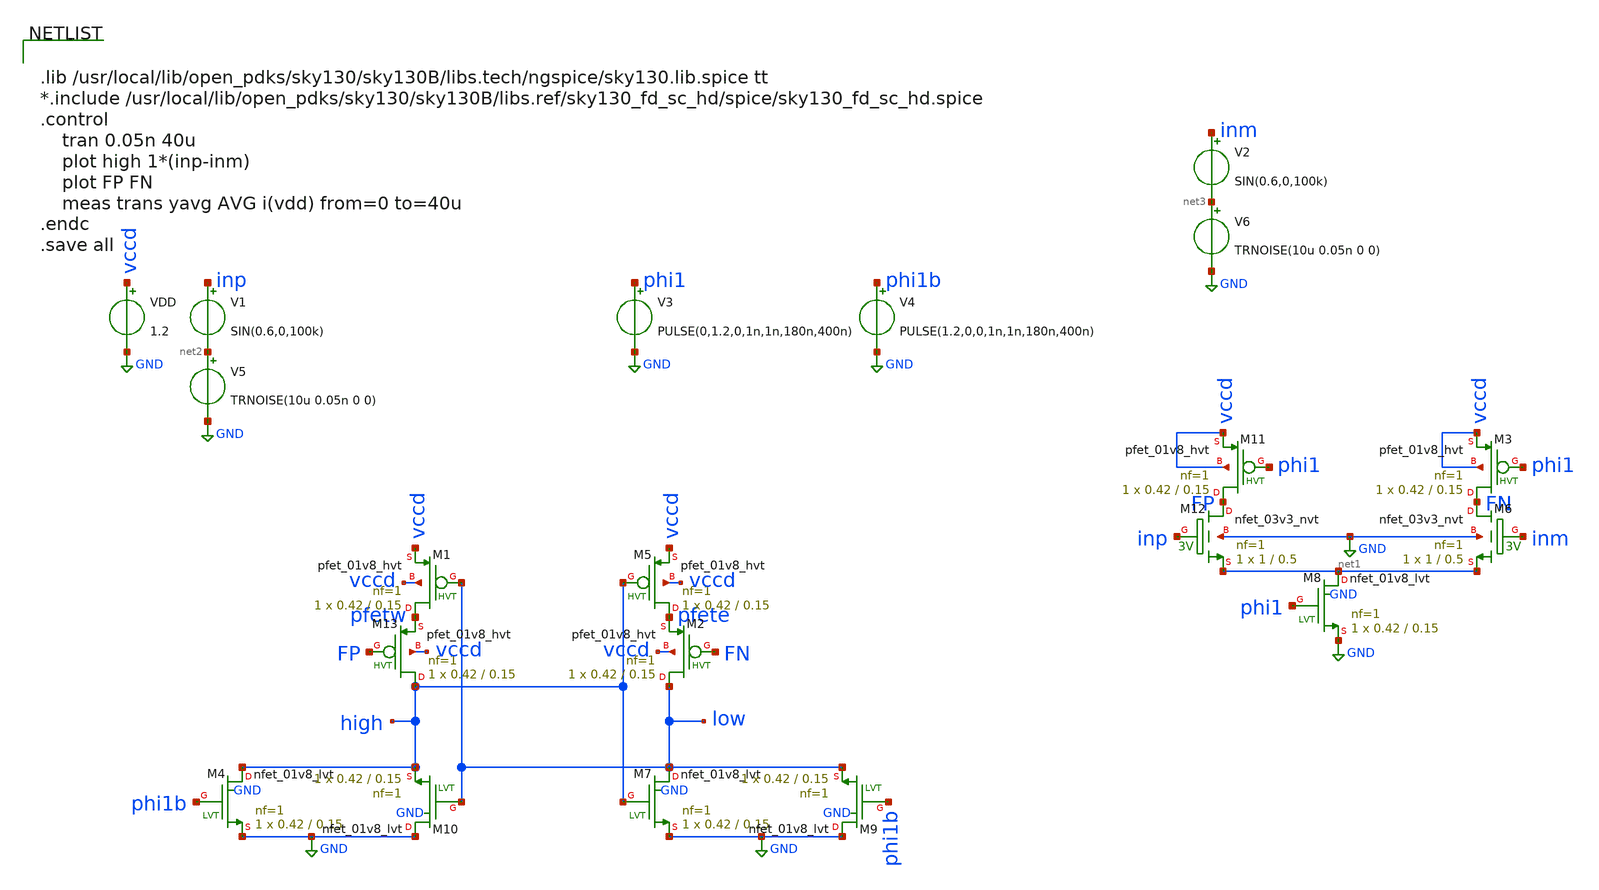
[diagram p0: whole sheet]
** sch_path: xschem/test_bench/comparator_tb.sch
**.subckt comparator_tb
V1 inp net2 SIN(0.6,0,100k)
VDD vccd GND 1.2
V2 inm net3 SIN(0.6,0,100k)
V3 phi1 GND PULSE(0,1.2,0,1n,1n,180n,400n)
V4 phi1b GND PULSE(1.2,0,0,1n,1n,180n,400n)
XM4 high phi1b GND GND sky130_fd_pr__nfet_01v8_lvt L=0.15 W=0.42 nf=1 ad='int((nf+1)/2) * W/nf * 0.29'
+ as='int((nf+2)/2) * W/nf * 0.29' pd='2*int((nf+1)/2) * (W/nf + 0.29)' ps='2*int((nf+2)/2) * (W/nf + 0.29)'
+ nrd='0.29 / W' nrs='0.29 / W' sa=0 sb=0 sd=0 mult=1 m=1
XM7 low high GND GND sky130_fd_pr__nfet_01v8_lvt L=0.15 W=0.42 nf=1 ad='int((nf+1)/2) * W/nf * 0.29'
+ as='int((nf+2)/2) * W/nf * 0.29' pd='2*int((nf+1)/2) * (W/nf + 0.29)' ps='2*int((nf+2)/2) * (W/nf + 0.29)'
+ nrd='0.29 / W' nrs='0.29 / W' sa=0 sb=0 sd=0 mult=1 m=1
XM9 GND phi1b low GND sky130_fd_pr__nfet_01v8_lvt L=0.15 W=0.42 nf=1 ad='int((nf+1)/2) * W/nf * 0.29'
+ as='int((nf+2)/2) * W/nf * 0.29' pd='2*int((nf+1)/2) * (W/nf + 0.29)' ps='2*int((nf+2)/2) * (W/nf + 0.29)'
+ nrd='0.29 / W' nrs='0.29 / W' sa=0 sb=0 sd=0 mult=1 m=1
XM10 GND low high GND sky130_fd_pr__nfet_01v8_lvt L=0.15 W=0.42 nf=1 ad='int((nf+1)/2) * W/nf * 0.29'
+ as='int((nf+2)/2) * W/nf * 0.29' pd='2*int((nf+1)/2) * (W/nf + 0.29)' ps='2*int((nf+2)/2) * (W/nf + 0.29)'
+ nrd='0.29 / W' nrs='0.29 / W' sa=0 sb=0 sd=0 mult=1 m=1
XM8 net1 phi1 GND GND sky130_fd_pr__nfet_01v8_lvt L=0.15 W=0.42 nf=1 ad='int((nf+1)/2) * W/nf * 0.29'
+ as='int((nf+2)/2) * W/nf * 0.29' pd='2*int((nf+1)/2) * (W/nf + 0.29)' ps='2*int((nf+2)/2) * (W/nf + 0.29)'
+ nrd='0.29 / W' nrs='0.29 / W' sa=0 sb=0 sd=0 mult=1 m=1
XM12 FP inp net1 GND sky130_fd_pr__nfet_03v3_nvt L=0.5 W=1 nf=1 ad='int((nf+1)/2) * W/nf * 0.29' as='int((nf+2)/2) * W/nf * 0.29'
+ pd='2*int((nf+1)/2) * (W/nf + 0.29)' ps='2*int((nf+2)/2) * (W/nf + 0.29)' nrd='0.29 / W' nrs='0.29 / W'
+ sa=0 sb=0 sd=0 mult=1 m=1
XM6 FN inm net1 GND sky130_fd_pr__nfet_03v3_nvt L=0.5 W=1 nf=1 ad='int((nf+1)/2) * W/nf * 0.29' as='int((nf+2)/2) * W/nf * 0.29'
+ pd='2*int((nf+1)/2) * (W/nf + 0.29)' ps='2*int((nf+2)/2) * (W/nf + 0.29)' nrd='0.29 / W' nrs='0.29 / W'
+ sa=0 sb=0 sd=0 mult=1 m=1
XM11 FP phi1 vccd vccd sky130_fd_pr__pfet_01v8_hvt L=0.15 W=0.42 nf=1 ad='int((nf+1)/2) * W/nf * 0.29'
+ as='int((nf+2)/2) * W/nf * 0.29' pd='2*int((nf+1)/2) * (W/nf + 0.29)' ps='2*int((nf+2)/2) * (W/nf + 0.29)'
+ nrd='0.29 / W' nrs='0.29 / W' sa=0 sb=0 sd=0 mult=1 m=1
XM3 FN phi1 vccd vccd sky130_fd_pr__pfet_01v8_hvt L=0.15 W=0.42 nf=1 ad='int((nf+1)/2) * W/nf * 0.29'
+ as='int((nf+2)/2) * W/nf * 0.29' pd='2*int((nf+1)/2) * (W/nf + 0.29)' ps='2*int((nf+2)/2) * (W/nf + 0.29)'
+ nrd='0.29 / W' nrs='0.29 / W' sa=0 sb=0 sd=0 mult=1 m=1
XM1 pfetw low vccd vccd sky130_fd_pr__pfet_01v8_hvt L=0.15 W=0.42 nf=1 ad='int((nf+1)/2) * W/nf * 0.29'
+ as='int((nf+2)/2) * W/nf * 0.29' pd='2*int((nf+1)/2) * (W/nf + 0.29)' ps='2*int((nf+2)/2) * (W/nf + 0.29)'
+ nrd='0.29 / W' nrs='0.29 / W' sa=0 sb=0 sd=0 mult=1 m=1
XM2 low FN pfete vccd sky130_fd_pr__pfet_01v8_hvt L=0.15 W=0.42 nf=1 ad='int((nf+1)/2) * W/nf * 0.29'
+ as='int((nf+2)/2) * W/nf * 0.29' pd='2*int((nf+1)/2) * (W/nf + 0.29)' ps='2*int((nf+2)/2) * (W/nf + 0.29)'
+ nrd='0.29 / W' nrs='0.29 / W' sa=0 sb=0 sd=0 mult=1 m=1
XM5 pfete high vccd vccd sky130_fd_pr__pfet_01v8_hvt L=0.15 W=0.42 nf=1 ad='int((nf+1)/2) * W/nf * 0.29'
+ as='int((nf+2)/2) * W/nf * 0.29' pd='2*int((nf+1)/2) * (W/nf + 0.29)' ps='2*int((nf+2)/2) * (W/nf + 0.29)'
+ nrd='0.29 / W' nrs='0.29 / W' sa=0 sb=0 sd=0 mult=1 m=1
XM13 high FP pfetw vccd sky130_fd_pr__pfet_01v8_hvt L=0.15 W=0.42 nf=1 ad='int((nf+1)/2) * W/nf * 0.29'
+ as='int((nf+2)/2) * W/nf * 0.29' pd='2*int((nf+1)/2) * (W/nf + 0.29)' ps='2*int((nf+2)/2) * (W/nf + 0.29)'
+ nrd='0.29 / W' nrs='0.29 / W' sa=0 sb=0 sd=0 mult=1 m=1
V5 net2 GND TRNOISE(10u 0.05n 0 0)
V6 net3 GND TRNOISE(10u 0.05n 0 0)
**** begin user architecture code


.lib /usr/local/lib/open_pdks/sky130/sky130B/libs.tech/ngspice/sky130.lib.spice tt
*.include /usr/local/lib/open_pdks/sky130/sky130B/libs.ref/sky130_fd_sc_hd/spice/sky130_fd_sc_hd.spice
.control
    tran 0.05n 40u
    plot high 1*(inp-inm)
    plot FP FN
    meas trans yavg AVG i(vdd) from=0 to=40u
.endc
.save all


**** end user architecture code
**.ends
.GLOBAL GND
.end
